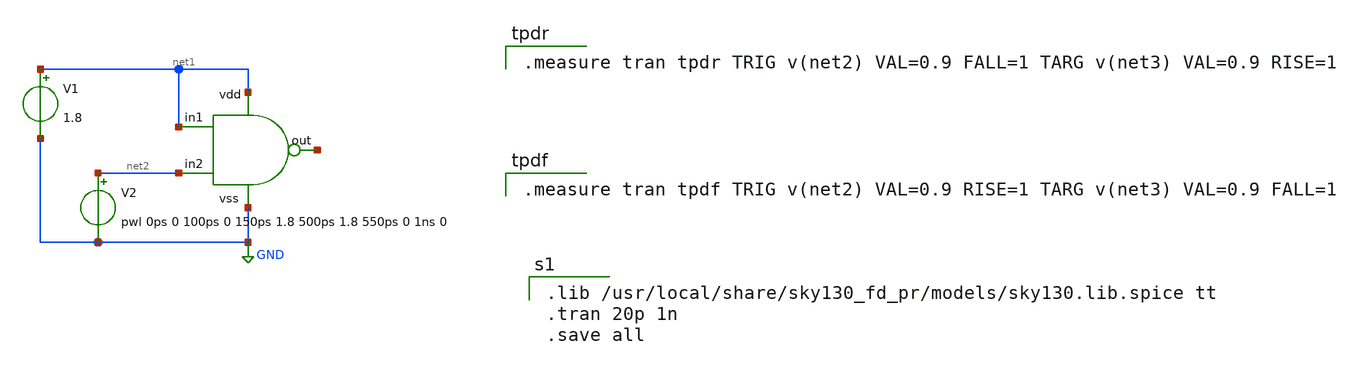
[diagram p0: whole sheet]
** sch_path: projects/carry_lookahead_adder/xschem/ports/test/rise_fall_time/nand.sch
**.subckt nand
V1 net1 GND 1.8
V2 net2 GND pwl 0ps 0 100ps 0 150ps 1.8 500ps 1.8 550ps 0 1ns 0
x1 net1 net2 net3 net1 GND nand
**** begin user architecture code

.lib /usr/local/share/sky130_fd_pr/models/sky130.lib.spice tt
.tran 20p 1n
.save all


.measure tran tpdr TRIG v(net2) VAL=0.9 FALL=1 TARG v(net3) VAL=0.9 RISE=1


.measure tran tpdf TRIG v(net2) VAL=0.9 RISE=1 TARG v(net3) VAL=0.9 FALL=1

**** end user architecture code
**.ends

* expanding   symbol:
*+  /home/peppe/Scrivania/vlsi/circuits-simulation/projects/carry_lookahead_adder/xschem/ports/nand.sym # of pins=5
** sym_path: projects/carry_lookahead_adder/xschem/ports/nand.sym
** sch_path: projects/carry_lookahead_adder/xschem/ports/nand.sch
.subckt nand in1 in2 out vdd vss
*.ipin in1
*.ipin in2
*.ipin vdd
*.ipin vss
*.opin out
XM1 net1 in2 vss vss sky130_fd_pr__nfet_01v8 L=0.15 W=2 nf=1 ad='int((nf+1)/2) * W/nf * 0.29' as='int((nf+2)/2) * W/nf * 0.29'
+ pd='2*int((nf+1)/2) * (W/nf + 0.29)' ps='2*int((nf+2)/2) * (W/nf + 0.29)' nrd='0.29 / W' nrs='0.29 / W'
+ sa=0 sb=0 sd=0 mult=1 m=1
XM2 out in1 net1 net1 sky130_fd_pr__nfet_01v8 L=0.15 W=2 nf=1 ad='int((nf+1)/2) * W/nf * 0.29' as='int((nf+2)/2) * W/nf * 0.29'
+ pd='2*int((nf+1)/2) * (W/nf + 0.29)' ps='2*int((nf+2)/2) * (W/nf + 0.29)' nrd='0.29 / W' nrs='0.29 / W'
+ sa=0 sb=0 sd=0 mult=1 m=1
XM6 out in1 vdd vdd sky130_fd_pr__pfet_01v8 L=0.15 W=3.8 nf=1 ad='int((nf+1)/2) * W/nf * 0.29' as='int((nf+2)/2) * W/nf * 0.29'
+ pd='2*int((nf+1)/2) * (W/nf + 0.29)' ps='2*int((nf+2)/2) * (W/nf + 0.29)' nrd='0.29 / W' nrs='0.29 / W'
+ sa=0 sb=0 sd=0 mult=1 m=1
XM3 out in2 vdd vdd sky130_fd_pr__pfet_01v8 L=0.15 W=3.8 nf=1 ad='int((nf+1)/2) * W/nf * 0.29' as='int((nf+2)/2) * W/nf * 0.29'
+ pd='2*int((nf+1)/2) * (W/nf + 0.29)' ps='2*int((nf+2)/2) * (W/nf + 0.29)' nrd='0.29 / W' nrs='0.29 / W'
+ sa=0 sb=0 sd=0 mult=1 m=1
.ends

.GLOBAL GND
.end
